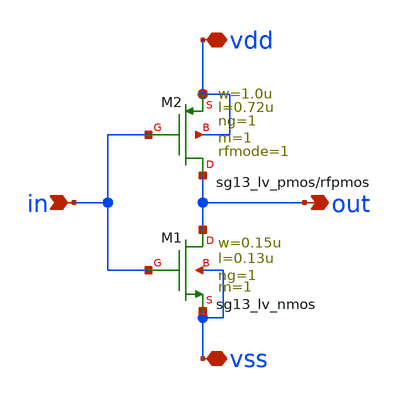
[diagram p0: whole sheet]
** sch_path: design/blocks/test-wf/schematic/inv.sch
**.subckt inv vdd vss out in
*.iopin vdd
*.iopin vss
*.opin out
*.ipin in
XM1 out in vss vss sg13_lv_nmos w=0.15u l=0.13u ng=1 m=1 mm_ok=1
XM2 out in vdd vdd sg13_lv_pmos w=1.0u l=0.72u ng=1 m=1 rfmode=1 mm_ok=1
**.ends
.end
